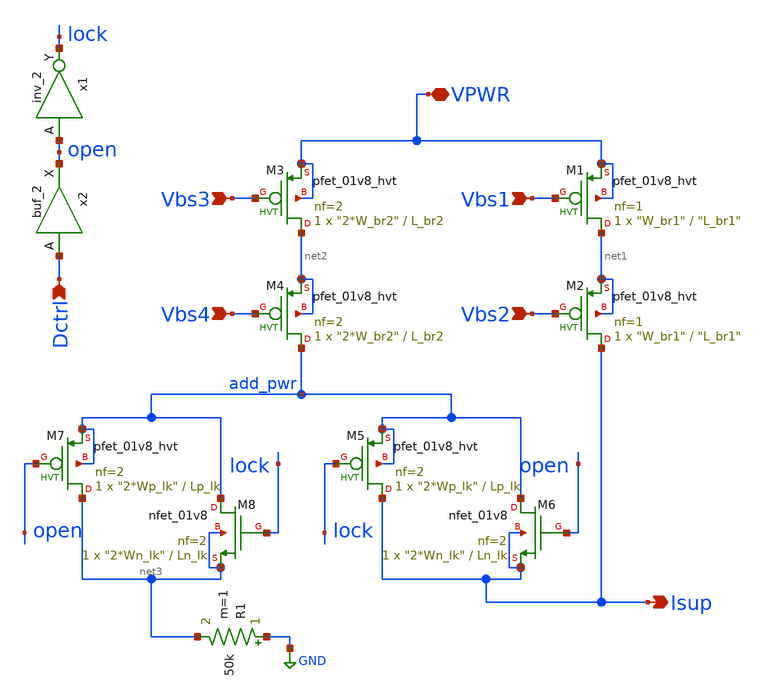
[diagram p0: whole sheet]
** sch_path: xschem/lib/ALib_IDAC.sch
**.subckt ALib_IDAC Vbs3 Vbs4 Vbs1 Vbs2 VPWR Isup Dctrl
*.ipin Vbs3
*.ipin Vbs4
*.ipin Vbs1
*.ipin Vbs2
*.iopin VPWR
*.opin Isup
*.ipin Dctrl
R1 GND net3 50k m=1
x1 open GND GND VPWR VPWR lock sky130_fd_sc_hd__inv_2
XM1 net1 Vbs1 VPWR VPWR sky130_fd_pr__pfet_01v8_hvt L="L_br1" W="W_br1" nf=1 ad='int((nf+1)/2) * W/nf * 0.29'
+ as='int((nf+2)/2) * W/nf * 0.29' pd='2*int((nf+1)/2) * (W/nf + 0.29)' ps='2*int((nf+2)/2) * (W/nf + 0.29)'
+ nrd='0.29 / W' nrs='0.29 / W' sa=0 sb=0 sd=0 mult=1 m=1
XM2 Isup Vbs2 net1 net1 sky130_fd_pr__pfet_01v8_hvt L="L_br1" W="W_br1" nf=1 ad='int((nf+1)/2) * W/nf * 0.29'
+ as='int((nf+2)/2) * W/nf * 0.29' pd='2*int((nf+1)/2) * (W/nf + 0.29)' ps='2*int((nf+2)/2) * (W/nf + 0.29)'
+ nrd='0.29 / W' nrs='0.29 / W' sa=0 sb=0 sd=0 mult=1 m=1
x2 Dctrl GND GND VPWR VPWR open sky130_fd_sc_hd__buf_2
XM3 net2 Vbs3 VPWR VPWR sky130_fd_pr__pfet_01v8_hvt L=L_br2 W="2*W_br2" nf=2 ad='int((nf+1)/2) * W/nf * 0.29'
+ as='int((nf+2)/2) * W/nf * 0.29' pd='2*int((nf+1)/2) * (W/nf + 0.29)' ps='2*int((nf+2)/2) * (W/nf + 0.29)'
+ nrd='0.29 / W' nrs='0.29 / W' sa=0 sb=0 sd=0 mult=1 m=1
XM4 add_pwr Vbs4 net2 net2 sky130_fd_pr__pfet_01v8_hvt L=L_br2 W="2*W_br2" nf=2 ad='int((nf+1)/2) * W/nf * 0.29'
+ as='int((nf+2)/2) * W/nf * 0.29' pd='2*int((nf+1)/2) * (W/nf + 0.29)' ps='2*int((nf+2)/2) * (W/nf + 0.29)'
+ nrd='0.29 / W' nrs='0.29 / W' sa=0 sb=0 sd=0 mult=1 m=1
XM5 Isup lock add_pwr add_pwr sky130_fd_pr__pfet_01v8_hvt L=Lp_lk W="2*Wp_lk" nf=2 ad='int((nf+1)/2) * W/nf * 0.29'
+ as='int((nf+2)/2) * W/nf * 0.29' pd='2*int((nf+1)/2) * (W/nf + 0.29)' ps='2*int((nf+2)/2) * (W/nf + 0.29)'
+ nrd='0.29 / W' nrs='0.29 / W' sa=0 sb=0 sd=0 mult=1 m=1
XM6 add_pwr open Isup Isup sky130_fd_pr__nfet_01v8 L=Ln_lk W="2*Wn_lk" nf=2 ad='int((nf+1)/2) * W/nf * 0.29'
+ as='int((nf+2)/2) * W/nf * 0.29' pd='2*int((nf+1)/2) * (W/nf + 0.29)' ps='2*int((nf+2)/2) * (W/nf + 0.29)'
+ nrd='0.29 / W' nrs='0.29 / W' sa=0 sb=0 sd=0 mult=1 m=1
XM7 net3 open add_pwr add_pwr sky130_fd_pr__pfet_01v8_hvt L=Lp_lk W="2*Wp_lk" nf=2 ad='int((nf+1)/2) * W/nf * 0.29'
+ as='int((nf+2)/2) * W/nf * 0.29' pd='2*int((nf+1)/2) * (W/nf + 0.29)' ps='2*int((nf+2)/2) * (W/nf + 0.29)'
+ nrd='0.29 / W' nrs='0.29 / W' sa=0 sb=0 sd=0 mult=1 m=1
XM8 add_pwr lock net3 net3 sky130_fd_pr__nfet_01v8 L=Ln_lk W="2*Wn_lk" nf=2 ad='int((nf+1)/2) * W/nf * 0.29'
+ as='int((nf+2)/2) * W/nf * 0.29' pd='2*int((nf+1)/2) * (W/nf + 0.29)' ps='2*int((nf+2)/2) * (W/nf + 0.29)'
+ nrd='0.29 / W' nrs='0.29 / W' sa=0 sb=0 sd=0 mult=1 m=1
**.ends
.GLOBAL GND
.end
